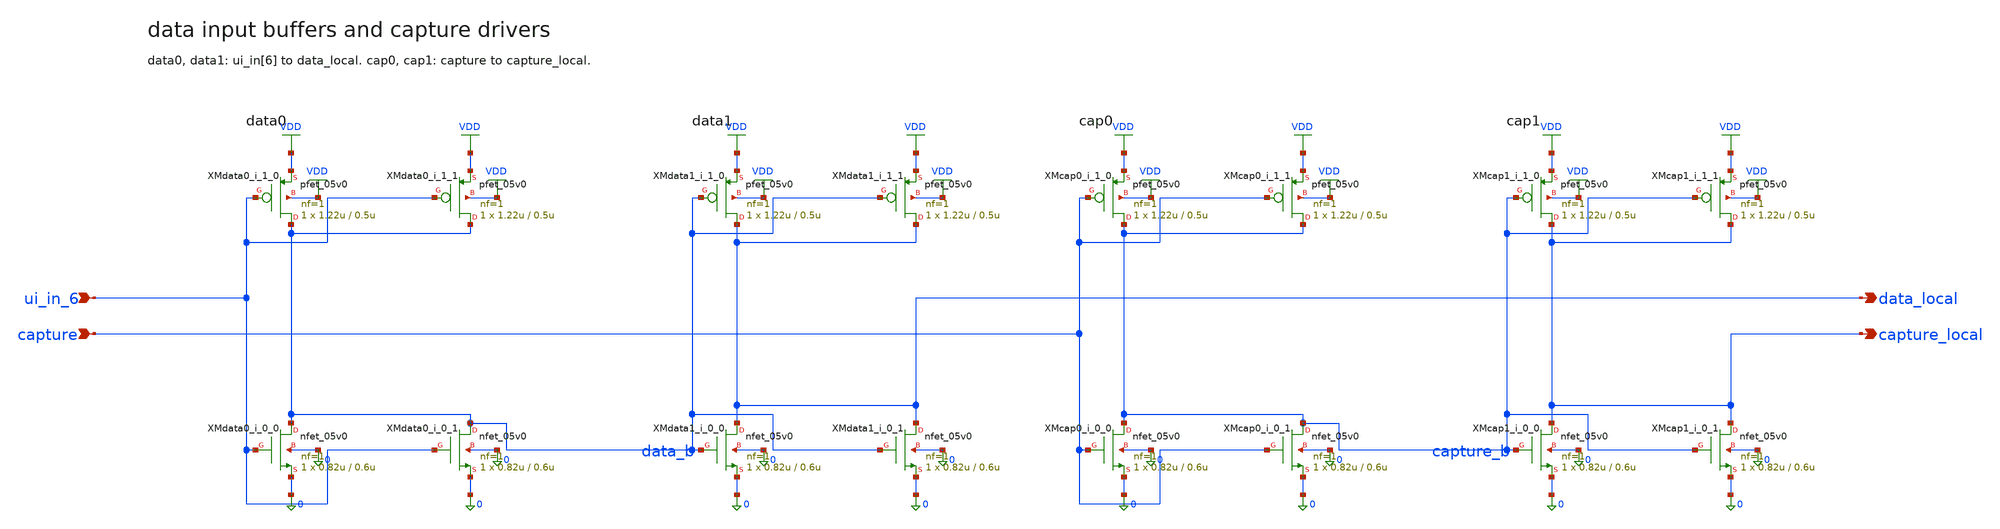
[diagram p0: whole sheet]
** sch_path: xschem/flat/data_and_capture.sch
**.subckt data_and_capture ui_in_6 capture data_local capture_local
*.ipin ui_in_6
*.ipin capture
*.opin data_local
*.opin capture_local
XMdata0_i_0_0 data_b ui_in_6 0 0 nfet_05v0 L=0.6u W=0.82u nf=1 ad=4.1e-13 as=4.1e-13 pd=2.64e-06
+ ps=2.64e-06 nrd=0 nrs=0 sa=0 sb=0 sd=0 m=1
XMdata0_i_0_1 data_b ui_in_6 0 0 nfet_05v0 L=0.6u W=0.82u nf=1 ad=4.1e-13 as=4.1e-13 pd=2.64e-06
+ ps=2.64e-06 nrd=0 nrs=0 sa=0 sb=0 sd=0 m=1
XMdata0_i_1_0 data_b ui_in_6 VDD VDD pfet_05v0 L=0.5u W=1.22u nf=1 ad=6.1e-13 as=6.1e-13 pd=3.44e-06
+ ps=3.44e-06 nrd=0 nrs=0 sa=0 sb=0 sd=0 m=1
XMdata0_i_1_1 data_b ui_in_6 VDD VDD pfet_05v0 L=0.5u W=1.22u nf=1 ad=6.1e-13 as=6.1e-13 pd=3.44e-06
+ ps=3.44e-06 nrd=0 nrs=0 sa=0 sb=0 sd=0 m=1
XMdata1_i_0_0 data_local data_b 0 0 nfet_05v0 L=0.6u W=0.82u nf=1 ad=4.1e-13 as=4.1e-13 pd=2.64e-06
+ ps=2.64e-06 nrd=0 nrs=0 sa=0 sb=0 sd=0 m=1
XMdata1_i_0_1 data_local data_b 0 0 nfet_05v0 L=0.6u W=0.82u nf=1 ad=4.1e-13 as=4.1e-13 pd=2.64e-06
+ ps=2.64e-06 nrd=0 nrs=0 sa=0 sb=0 sd=0 m=1
XMdata1_i_1_0 data_local data_b VDD VDD pfet_05v0 L=0.5u W=1.22u nf=1 ad=6.1e-13 as=6.1e-13
+ pd=3.44e-06 ps=3.44e-06 nrd=0 nrs=0 sa=0 sb=0 sd=0 m=1
XMdata1_i_1_1 data_local data_b VDD VDD pfet_05v0 L=0.5u W=1.22u nf=1 ad=6.1e-13 as=6.1e-13
+ pd=3.44e-06 ps=3.44e-06 nrd=0 nrs=0 sa=0 sb=0 sd=0 m=1
XMcap0_i_0_0 capture_b capture 0 0 nfet_05v0 L=0.6u W=0.82u nf=1 ad=4.1e-13 as=4.1e-13 pd=2.64e-06
+ ps=2.64e-06 nrd=0 nrs=0 sa=0 sb=0 sd=0 m=1
XMcap0_i_0_1 capture_b capture 0 0 nfet_05v0 L=0.6u W=0.82u nf=1 ad=4.1e-13 as=4.1e-13 pd=2.64e-06
+ ps=2.64e-06 nrd=0 nrs=0 sa=0 sb=0 sd=0 m=1
XMcap0_i_1_0 capture_b capture VDD VDD pfet_05v0 L=0.5u W=1.22u nf=1 ad=6.1e-13 as=6.1e-13
+ pd=3.44e-06 ps=3.44e-06 nrd=0 nrs=0 sa=0 sb=0 sd=0 m=1
XMcap0_i_1_1 capture_b capture VDD VDD pfet_05v0 L=0.5u W=1.22u nf=1 ad=6.1e-13 as=6.1e-13
+ pd=3.44e-06 ps=3.44e-06 nrd=0 nrs=0 sa=0 sb=0 sd=0 m=1
XMcap1_i_0_0 capture_local capture_b 0 0 nfet_05v0 L=0.6u W=0.82u nf=1 ad=4.1e-13 as=4.1e-13
+ pd=2.64e-06 ps=2.64e-06 nrd=0 nrs=0 sa=0 sb=0 sd=0 m=1
XMcap1_i_0_1 capture_local capture_b 0 0 nfet_05v0 L=0.6u W=0.82u nf=1 ad=4.1e-13 as=4.1e-13
+ pd=2.64e-06 ps=2.64e-06 nrd=0 nrs=0 sa=0 sb=0 sd=0 m=1
XMcap1_i_1_0 capture_local capture_b VDD VDD pfet_05v0 L=0.5u W=1.22u nf=1 ad=6.1e-13 as=6.1e-13
+ pd=3.44e-06 ps=3.44e-06 nrd=0 nrs=0 sa=0 sb=0 sd=0 m=1
XMcap1_i_1_1 capture_local capture_b VDD VDD pfet_05v0 L=0.5u W=1.22u nf=1 ad=6.1e-13 as=6.1e-13
+ pd=3.44e-06 ps=3.44e-06 nrd=0 nrs=0 sa=0 sb=0 sd=0 m=1
**.ends
.GLOBAL VDD
.end
